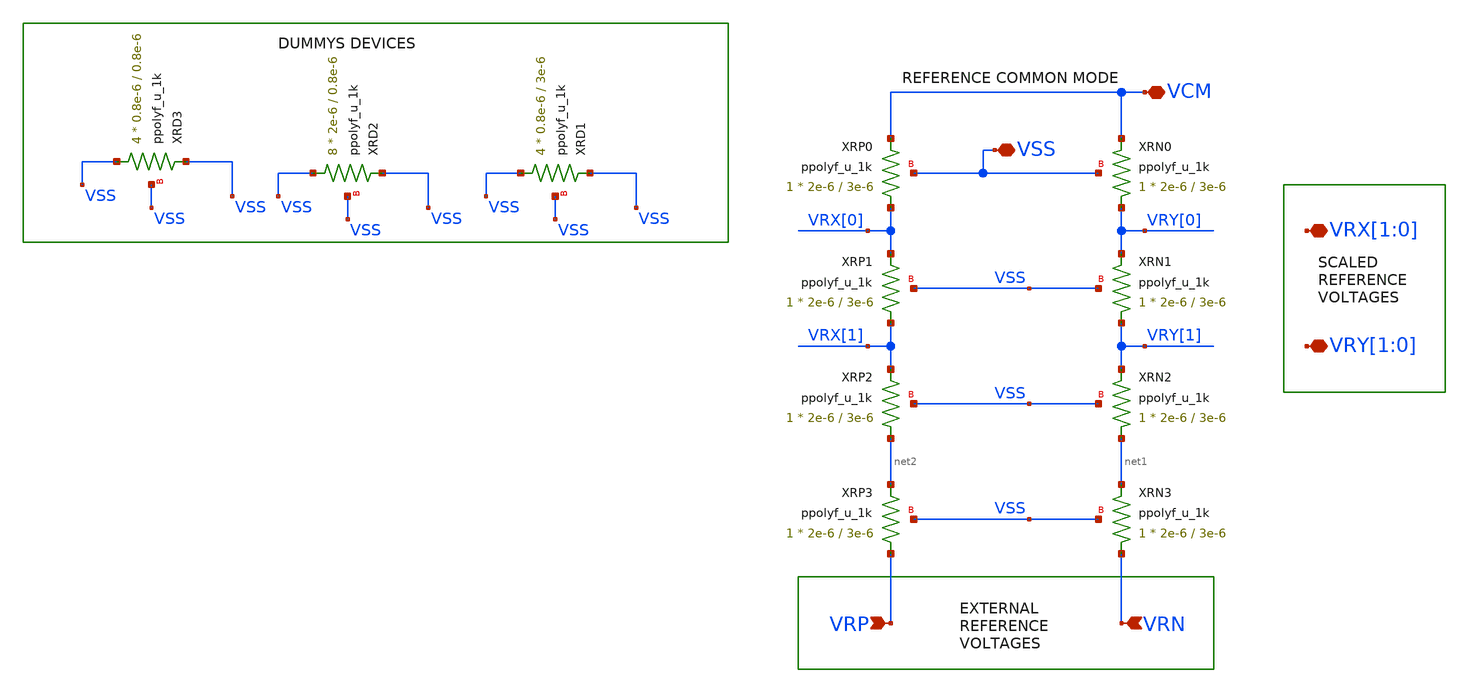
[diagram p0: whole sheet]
** sch_path: designs/sar_adc/dac/rdac/xschem/rdac.sch
**.subckt rdac VRN VRP VCM VRY[1],VRY[0] VRX[1],VRX[0] VSS
*.ipin VRN
*.ipin VRP
*.iopin VCM
*.iopin VRY[1],VRY[0]
*.iopin VRX[1],VRX[0]
*.iopin VSS
XRN0 VRY[0] VCM VSS ppolyf_u_1k r_width=2e-6 r_length=3e-6 m=1
XRN1 VRY[1] VRY[0] VSS ppolyf_u_1k r_width=2e-6 r_length=3e-6 m=1
XRN2 net1 VRY[1] VSS ppolyf_u_1k r_width=2e-6 r_length=3e-6 m=1
XRN3 VRN net1 VSS ppolyf_u_1k r_width=2e-6 r_length=3e-6 m=1
XRP0 VRX[0] VCM VSS ppolyf_u_1k r_width=2e-6 r_length=3e-6 m=1
XRP1 VRX[1] VRX[0] VSS ppolyf_u_1k r_width=2e-6 r_length=3e-6 m=1
XRP2 net2 VRX[1] VSS ppolyf_u_1k r_width=2e-6 r_length=3e-6 m=1
XRP3 VRP net2 VSS ppolyf_u_1k r_width=2e-6 r_length=3e-6 m=1
XRD1 VSS VSS VSS ppolyf_u_1k r_width=0.8e-6 r_length=3e-6 m=4
XRD2 VSS VSS VSS ppolyf_u_1k r_width=2e-6 r_length=0.8e-6 m=8
XRD3 VSS VSS VSS ppolyf_u_1k r_width=0.8e-6 r_length=0.8e-6 m=4
**.ends
.end
